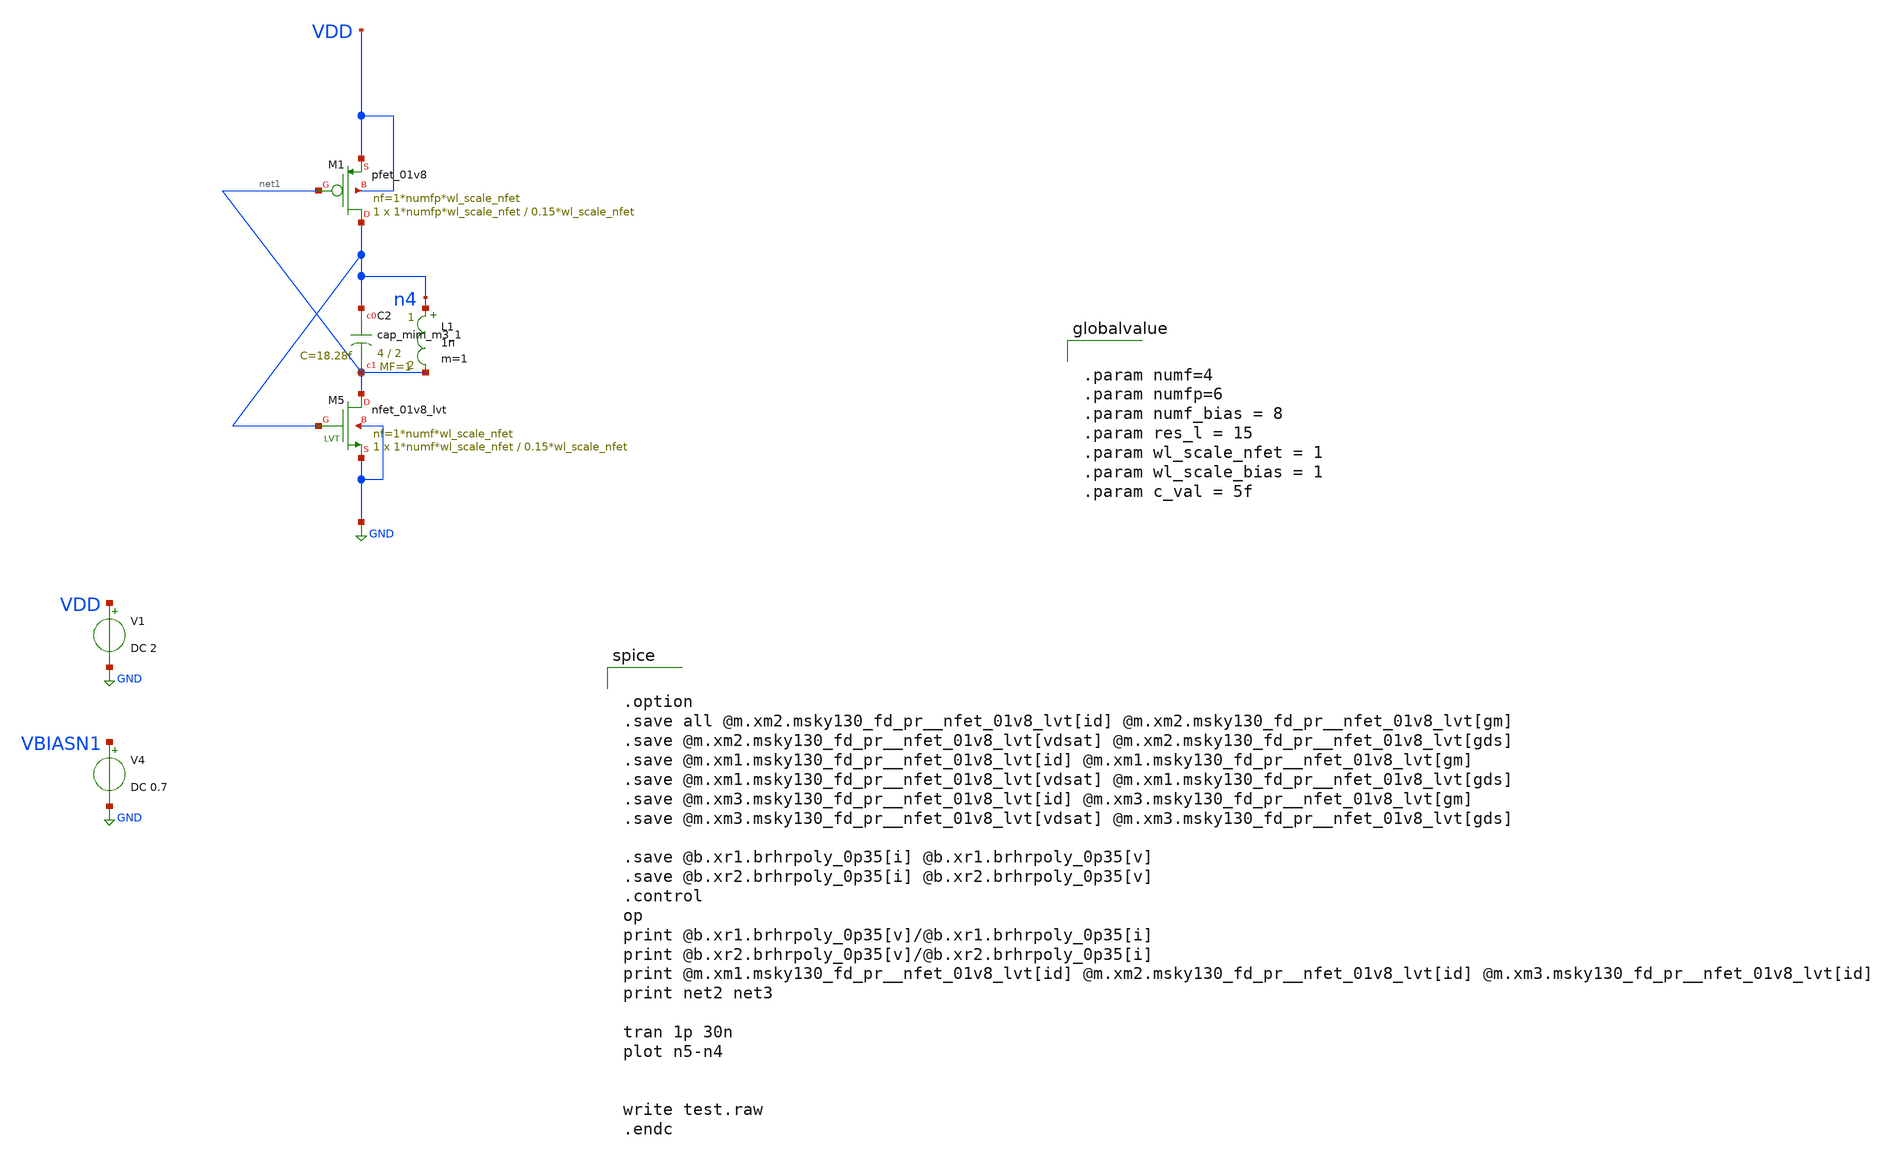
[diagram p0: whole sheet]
** sch_path: xschem/vco/test_amp2.sch
**.subckt test_amp2
V1 VDD GND DC 2
V4 VBIASN1 GND DC 0.7
XM5 net1 n4 GND GND sky130_fd_pr__nfet_01v8_lvt L=0.15*wl_scale_nfet W=1*numf*wl_scale_nfet nf=1*numf*wl_scale_nfet
+ ad='int((nf+1)/2) * W/nf * 0.29' as='int((nf+2)/2) * W/nf * 0.29' pd='2*int((nf+1)/2) * (W/nf + 0.29)'
+ ps='2*int((nf+2)/2) * (W/nf + 0.29)' nrd='0.29 / W' nrs='0.29 / W' sa=0 sb=0 sd=0 mult=1 m=1
L1 n4 net1 1n m=1
XC2 n4 net1 sky130_fd_pr__cap_mim_m3_1 W=4 L=2 MF=1 m=1
XM1 n4 net1 VDD VDD sky130_fd_pr__pfet_01v8 L=0.15*wl_scale_nfet W=1*numfp*wl_scale_nfet nf=1*numfp*wl_scale_nfet
+ ad='int((nf+1)/2) * W/nf * 0.29' as='int((nf+2)/2) * W/nf * 0.29' pd='2*int((nf+1)/2) * (W/nf + 0.29)'
+ ps='2*int((nf+2)/2) * (W/nf + 0.29)' nrd='0.29 / W' nrs='0.29 / W' sa=0 sb=0 sd=0 mult=1 m=1
**** begin user architecture code

** opencircuitdesign pdks install
.lib $::SKYWATER_MODELS/sky130.lib.spice tt_mm




.option
.save all @m.xm2.msky130_fd_pr__nfet_01v8_lvt[id] @m.xm2.msky130_fd_pr__nfet_01v8_lvt[gm]
.save @m.xm2.msky130_fd_pr__nfet_01v8_lvt[vdsat] @m.xm2.msky130_fd_pr__nfet_01v8_lvt[gds]
.save @m.xm1.msky130_fd_pr__nfet_01v8_lvt[id] @m.xm1.msky130_fd_pr__nfet_01v8_lvt[gm]
.save @m.xm1.msky130_fd_pr__nfet_01v8_lvt[vdsat] @m.xm1.msky130_fd_pr__nfet_01v8_lvt[gds]
.save @m.xm3.msky130_fd_pr__nfet_01v8_lvt[id] @m.xm3.msky130_fd_pr__nfet_01v8_lvt[gm]
.save @m.xm3.msky130_fd_pr__nfet_01v8_lvt[vdsat] @m.xm3.msky130_fd_pr__nfet_01v8_lvt[gds]

.save @b.xr1.brhrpoly_0p35[i] @b.xr1.brhrpoly_0p35[v]
.save @b.xr2.brhrpoly_0p35[i] @b.xr2.brhrpoly_0p35[v]
.control
op
print @b.xr1.brhrpoly_0p35[v]/@b.xr1.brhrpoly_0p35[i]
print @b.xr2.brhrpoly_0p35[v]/@b.xr2.brhrpoly_0p35[i]
print @m.xm1.msky130_fd_pr__nfet_01v8_lvt[id] @m.xm2.msky130_fd_pr__nfet_01v8_lvt[id]
+ @m.xm3.msky130_fd_pr__nfet_01v8_lvt[id]
print net2 net3

tran 1p 30n
plot n5-n4


write test.raw
.endc




.param numf=4
.param numfp=6
.param numf_bias = 8
.param res_l = 15
.param wl_scale_nfet = 1
.param wl_scale_bias = 1
.param c_val = 5f


**** end user architecture code
**.ends
.GLOBAL GND
.end
